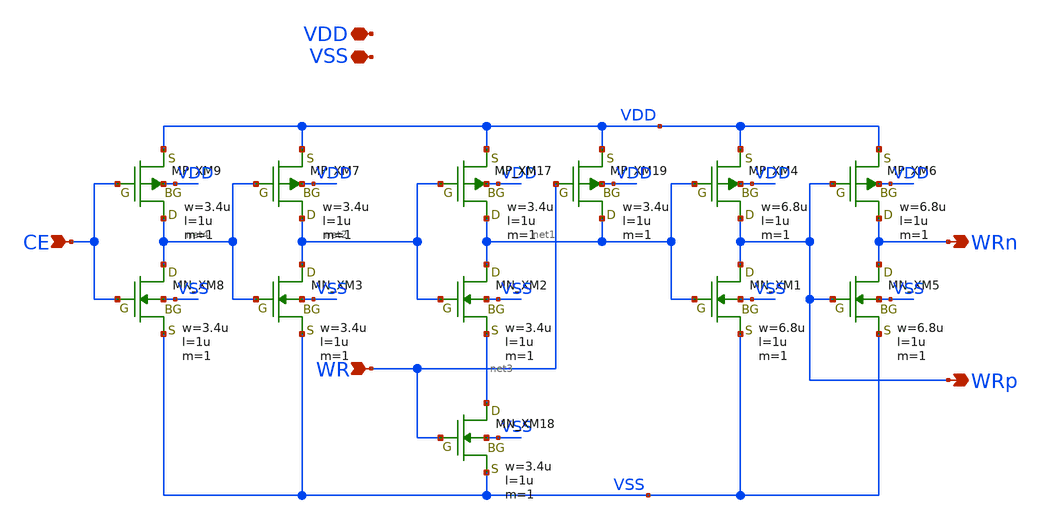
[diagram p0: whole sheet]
** sch_path: module/SRAM128/schematic/WRCTR.sch
**.subckt WRCTR WRn CE VDD VSS WR WRp
*.opin WRn
*.ipin CE
*.iopin VDD
*.iopin VSS
*.ipin WR
*.opin WRp
XXM1 WRp net1 VSS VSS NMOS w=6.8u l=1u as=0 ad=0 ps=0 pd=0 nrd=0 nrs=0 m=1
XXM4 WRp net1 VDD VDD PMOS w=6.8u l=1u as=0 ad=0 ps=0 pd=0 nrd=0 nrs=0 m=1
XXM2 net1 net2 net3 VSS NMOS w=3.4u l=1u as=0 ad=0 ps=0 pd=0 nrd=0 nrs=0 m=1
XXM17 net1 net2 VDD VDD PMOS w=3.4u l=1u as=0 ad=0 ps=0 pd=0 nrd=0 nrs=0 m=1
XXM18 net3 WR VSS VSS NMOS w=3.4u l=1u as=0 ad=0 ps=0 pd=0 nrd=0 nrs=0 m=1
XXM19 net1 WR VDD VDD PMOS w=3.4u l=1u as=0 ad=0 ps=0 pd=0 nrd=0 nrs=0 m=1
XXM5 WRn WRp VSS VSS NMOS w=6.8u l=1u as=0 ad=0 ps=0 pd=0 nrd=0 nrs=0 m=1
XXM6 WRn WRp VDD VDD PMOS w=6.8u l=1u as=0 ad=0 ps=0 pd=0 nrd=0 nrs=0 m=1
XXM3 net2 net4 VSS VSS NMOS w=3.4u l=1u as=0 ad=0 ps=0 pd=0 nrd=0 nrs=0 m=1
XXM7 net2 net4 VDD VDD PMOS w=3.4u l=1u as=0 ad=0 ps=0 pd=0 nrd=0 nrs=0 m=1
XXM8 net4 CE VSS VSS NMOS w=3.4u l=1u as=0 ad=0 ps=0 pd=0 nrd=0 nrs=0 m=1
XXM9 net4 CE VDD VDD PMOS w=3.4u l=1u as=0 ad=0 ps=0 pd=0 nrd=0 nrs=0 m=1
**.ends
.end
